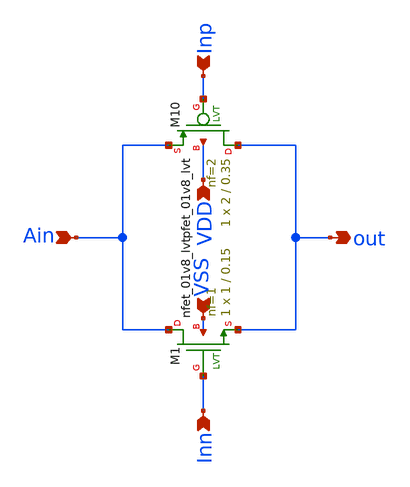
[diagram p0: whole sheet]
** sch_path: xschem/pass_gate.sch
**.subckt pass_gate Inp Inn out Ain VDD VSS
*.ipin Inp
*.ipin Inn
*.opin out
*.ipin Ain
*.ipin VDD
*.ipin VSS
XM10 out Inp Ain VDD sky130_fd_pr__pfet_01v8_lvt L=0.35 W=2 nf=2 ad='int((2 + 1)/2) * 2 / 2 * 0.29' as='int((2 + 2)/2) * 2 / 2 * 0.29'
+ pd='2*int((2 + 1)/2) * (2 / 2 + 0.29)' ps='2*int((2 + 2)/2) * (2 / 2 + 0.29)' nrd='0.29 / 2 ' nrs='0.29 / 2 '
+ sa=0 sb=0 sd=0 mult=1 m=1
XM1 Ain Inn out VSS sky130_fd_pr__nfet_01v8_lvt L=0.15 W=1 nf=1 ad='int((1 + 1)/2) * 1 / 1 * 0.29' as='int((1 + 2)/2) * 1 / 1 * 0.29'
+ pd='2*int((1 + 1)/2) * (1 / 1 + 0.29)' ps='2*int((1 + 2)/2) * (1 / 1 + 0.29)' nrd='0.29 / 1 ' nrs='0.29 / 1 '
+ sa=0 sb=0 sd=0 mult=1 m=1
**.ends
.end
